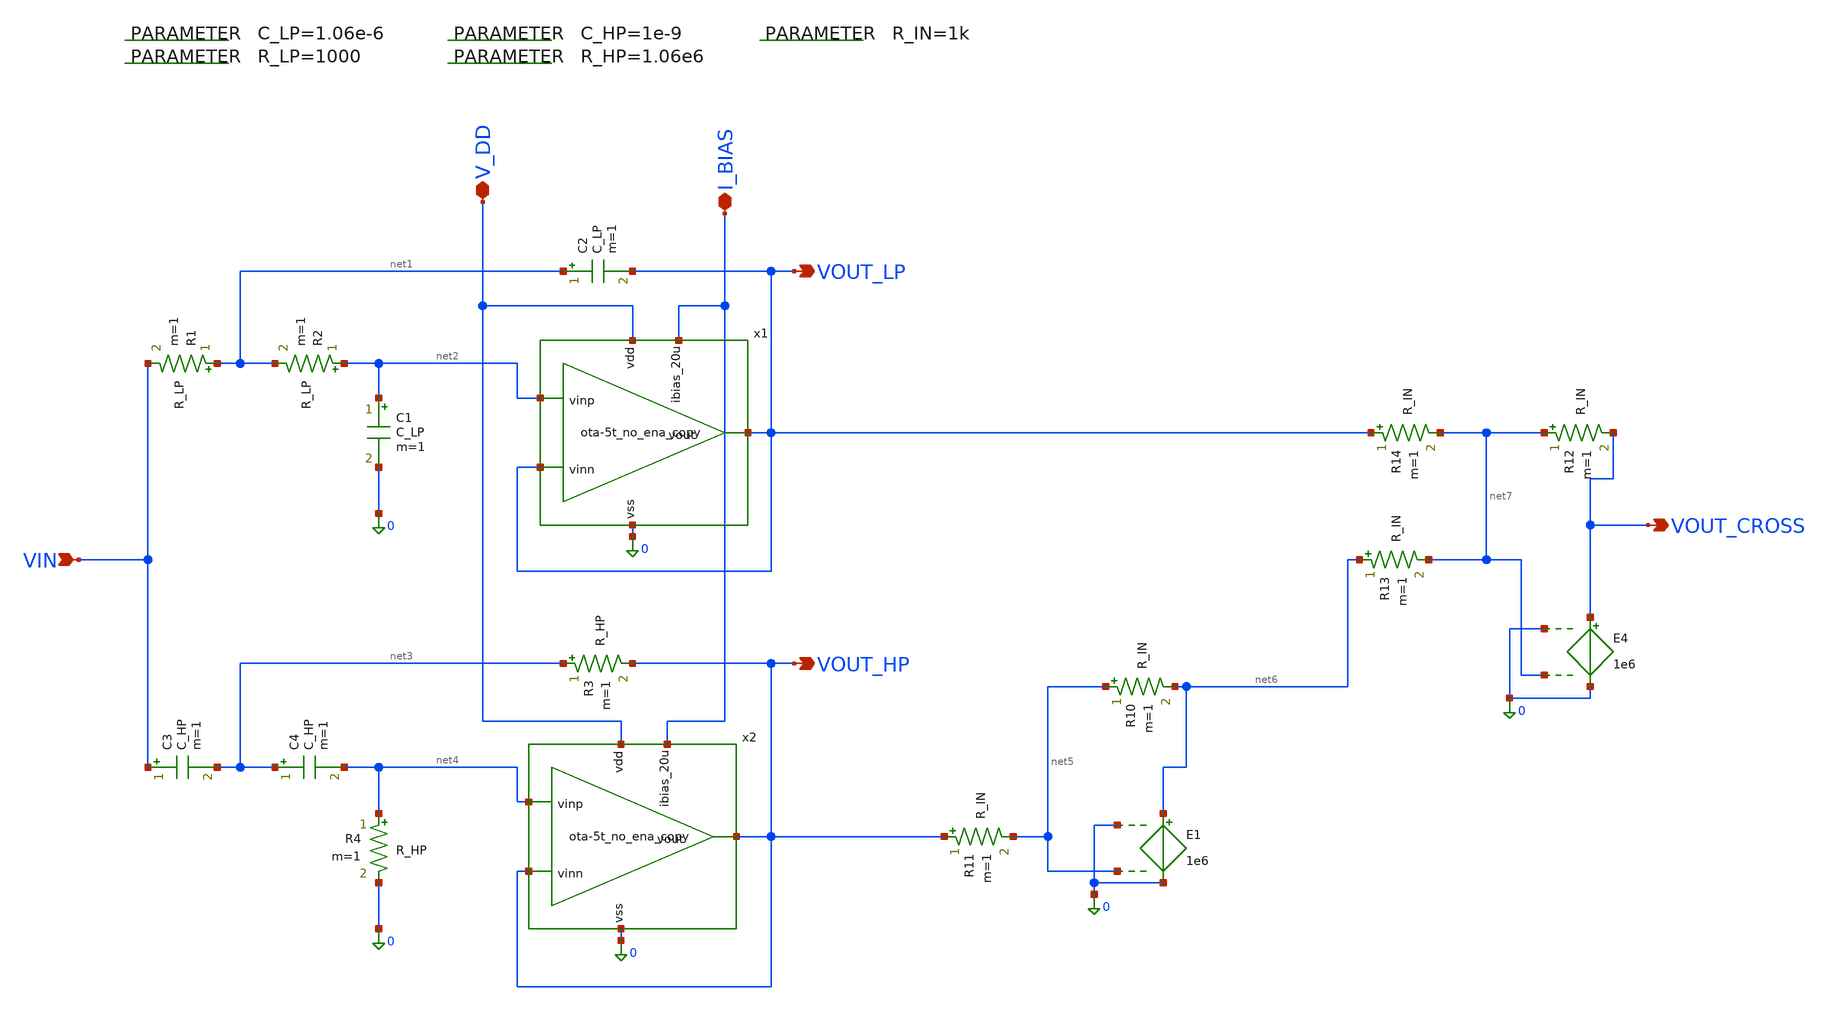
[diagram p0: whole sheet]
** sch_path: 004_Real_Circuits/version_no_enable/linkwtz_riley_crossover_pretl_OTA.sch
**.subckt linkwtz_riley_crossover_pretl_OTA VOUT_LP VOUT_HP VIN I_BIAS V_DD VOUT_CROSS
*.opin VOUT_LP
*.opin VOUT_HP
*.ipin VIN
*.iopin I_BIAS
*.iopin V_DD
*.opin VOUT_CROSS
R1 net1 VIN R_LP m=1
.param C_LP=1.06e-6
.param R_LP=1000
.param C_HP=1e-9
.param R_HP=1.06e6
.param R_IN=1k
R2 net2 net1 R_LP m=1
C1 net2 0 C_LP m=1
C2 net1 VOUT_LP C_LP m=1
C3 VIN net3 C_HP m=1
C4 net3 net4 C_HP m=1
R3 net3 VOUT_HP R_HP m=1
R4 net4 0 R_HP m=1
R10 net5 net6 R_IN m=1
R11 VOUT_HP net5 R_IN m=1
R12 net7 VOUT_CROSS R_IN m=1
R13 net6 net7 R_IN m=1
R14 VOUT_LP net7 R_IN m=1
E1 net6 0 0 net5 1e6
E4 VOUT_CROSS 0 0 net7 1e6
x1 V_DD VOUT_LP net2 VOUT_LP I_BIAS 0 ota-5t_no_ena_copy
x2 V_DD VOUT_HP net4 VOUT_HP I_BIAS 0 ota-5t_no_ena_copy
**.ends

* expanding   symbol:  /foss/designs/real_circuit/ota-5t_no_ena_copy.sym # of pins=6
** sym_path: 004_Real_Circuits/version_no_enable/ota-5t_no_ena_copy.sym
** sch_path: 004_Real_Circuits/version_no_enable/ota-5t_no_ena_copy.sch
.subckt ota-5t_no_ena_copy vdd vout vinp vinn ibias_20u vss
*.opin vout
*.iopin vdd
*.ipin vinp
*.ipin vinn
*.ipin ibias_20u
*.iopin vss
XM5 tail ibias_20u vss vss sg13_lv_nmos w=1.0u l=5u ng=1 m=1 mm_ok=1
XM4 vout gate_p vdd vdd sg13_lv_pmos w=2.5u l=5u ng=1 m=1 mm_ok=1
XM1 gate_p vinp tail vss sg13_lv_nmos w=2u l=5u ng=1 m=1 mm_ok=1
XM2 vout vinn tail vss sg13_lv_nmos w=2u l=5u ng=1 m=1 mm_ok=1
XM3 gate_p gate_p vdd vdd sg13_lv_pmos w=2.5u l=5u ng=1 m=1 mm_ok=1
XM6 ibias_20u ibias_20u vss vss sg13_lv_nmos w=6.5u l=5u ng=5 m=1 mm_ok=1
.ends

.end
